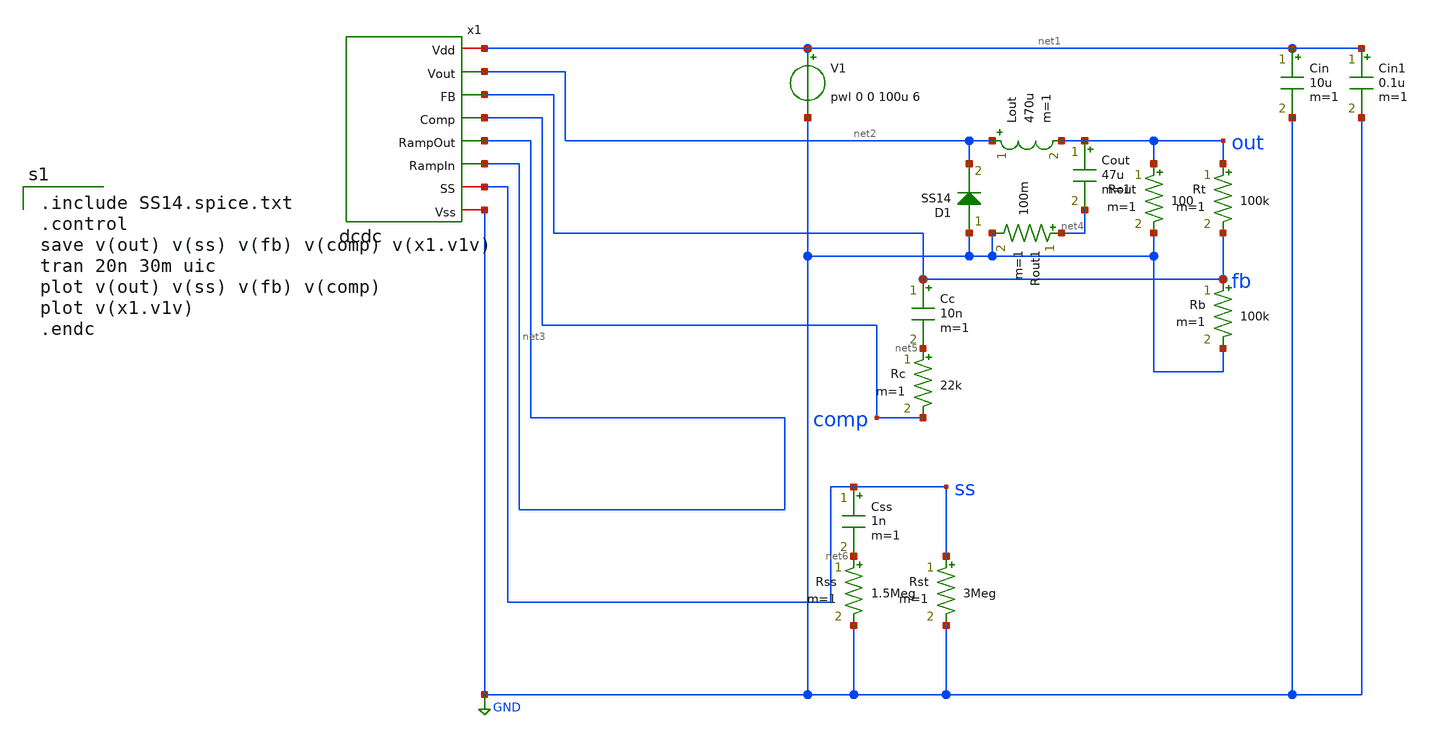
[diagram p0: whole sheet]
** sch_path: member_project/DCDC/xschem/dcdc_tran_nopin.sch
**.subckt dcdc_tran_nopin
x1 net1 ss net2 net3 fb net3 GND comp dcdc
V1 net1 GND pwl 0 0 100u 6
D1 GND net2 SS14 area=1
Lout net2 out 470u m=1
Cout out net4 47u m=1
Rout out GND 100 m=1
Rt out fb 100k m=1
Rb fb GND 100k m=1
Rc net5 comp 22k m=1
Cc fb net5 10n m=1
Css ss net6 1n m=1
Rss net6 GND 1.5Meg m=1
Rst ss GND 3Meg m=1
Rout1 net4 GND 100m m=1
Cin net1 GND 10u m=1
Cin1 net1 GND 0.1u m=1
**** begin user architecture code
 .include $::LIB/ip62_models

.include SS14.spice.txt
.control
save v(out) v(ss) v(fb) v(comp) v(x1.v1v)
tran 20n 30m uic
plot v(out) v(ss) v(fb) v(comp)
plot v(x1.v1v)
.endc

**** end user architecture code
**.ends
.GLOBAL GND
.end
